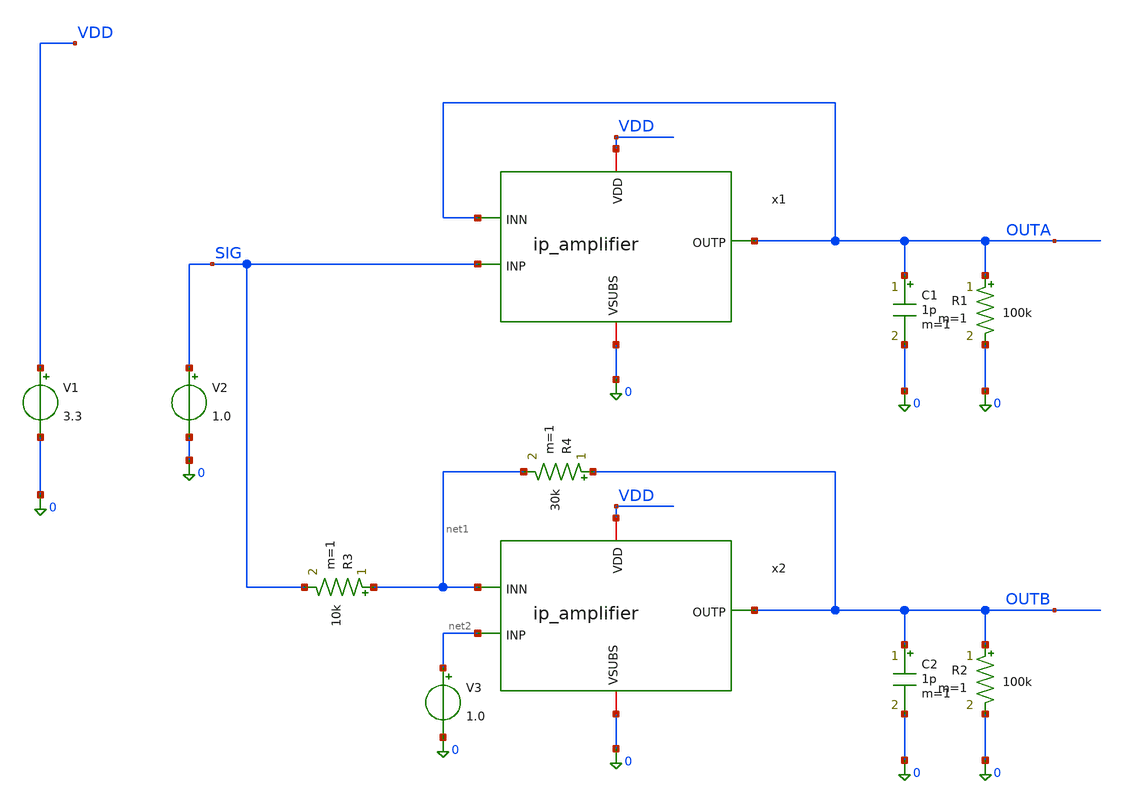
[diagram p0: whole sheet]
** sch_path: xschem/tb_amplifier_dc.sch
**.subckt tb_amplifier_dc
V1 VDD 0 3.3
x1 VDD OUTA SIG OUTA 0 ip_amplifier
V2 SIG 0 1.0
R1 OUTA 0 100k m=1
C1 OUTA 0 1p m=1
x2 VDD OUTB net2 net1 0 ip_amplifier
R2 OUTB 0 100k m=1
C2 OUTB 0 1p m=1
V3 net2 0 1.0
R3 net1 SIG 10k m=1
R4 OUTB net1 30k m=1
**** begin user architecture code

.lib $::180MCU_MODELS/sm141064.ngspice statistical
.lib $::180MCU_MODELS/sm141064.ngspice res_statistical
.lib $::180MCU_MODELS/sm141064.ngspice moscap_typical
.lib $::180MCU_MODELS/sm141064.ngspice diode_typical




.param sw_stat_global   = 1
.param sw_stat_mismatch = 1
.param mc_skew          = 1
.param res_mc_skew=3
.param cap_mc_skew=3
.param fnoicor=0

.control
	save all
	repeat 1
		mc_source
		dc V2 0 2 0.01
		write tb_amplifier_dc.raw
		set appendwrite
		reset
	end
	quit
.endc



**** end user architecture code
**.ends

* expanding   symbol:  ip_amplifier.sym # of pins=5
** sym_path: xschem/ip_amplifier.sym
** sch_path: xschem/ip_amplifier.sch
.subckt ip_amplifier VDD OUTP INP INN VSUBS
*.iopin VDD
*.iopin VSUBS
*.ipin INP
*.ipin INN
*.opin OUTP
XM1 net9 INP net7 VDD pfet_06v0 L=2u W=40u nf=1 ad='int((nf+1)/2) * W/nf * 0.18u' as='int((nf+2)/2) * W/nf * 0.18u'
+ pd='2*int((nf+1)/2) * (W/nf + 0.18u)' ps='2*int((nf+2)/2) * (W/nf + 0.18u)' nrd='0.18u / W' nrs='0.18u / W'
+ sa=0 sb=0 sd=0 m=1 par=1
XM2 net8 INN net7 VDD pfet_06v0 L=2u W=40u nf=1 ad='int((nf+1)/2) * W/nf * 0.18u' as='int((nf+2)/2) * W/nf * 0.18u'
+ pd='2*int((nf+1)/2) * (W/nf + 0.18u)' ps='2*int((nf+2)/2) * (W/nf + 0.18u)' nrd='0.18u / W' nrs='0.18u / W'
+ sa=0 sb=0 sd=0 m=1 par=1
XM5 net9 net1 VSUBS vsubs nfet_06v0 L=5u W=10u nf=1 ad='int((nf+1)/2) * W/nf * 0.18u' as='int((nf+2)/2) * W/nf * 0.18u'
+ pd='2*int((nf+1)/2) * (W/nf + 0.18u)' ps='2*int((nf+2)/2) * (W/nf + 0.18u)' nrd='0.18u / W' nrs='0.18u / W'
+ sa=0 sb=0 sd=0 m=1 par=1
XM6 net8 net1 VSUBS vsubs nfet_06v0 L=5u W=10u nf=1 ad='int((nf+1)/2) * W/nf * 0.18u' as='int((nf+2)/2) * W/nf * 0.18u'
+ pd='2*int((nf+1)/2) * (W/nf + 0.18u)' ps='2*int((nf+2)/2) * (W/nf + 0.18u)' nrd='0.18u / W' nrs='0.18u / W'
+ sa=0 sb=0 sd=0 m=1 par=1
XM3 net3 net1 VSUBS vsubs nfet_06v0 L=5u W=10u nf=1 ad='int((nf+1)/2) * W/nf * 0.18u' as='int((nf+2)/2) * W/nf * 0.18u'
+ pd='2*int((nf+1)/2) * (W/nf + 0.18u)' ps='2*int((nf+2)/2) * (W/nf + 0.18u)' nrd='0.18u / W' nrs='0.18u / W'
+ sa=0 sb=0 sd=0 m=1 par=1
XM4 net2 net1 VSUBS vsubs nfet_06v0 L=5u W=10u nf=1 ad='int((nf+1)/2) * W/nf * 0.18u' as='int((nf+2)/2) * W/nf * 0.18u'
+ pd='2*int((nf+1)/2) * (W/nf + 0.18u)' ps='2*int((nf+2)/2) * (W/nf + 0.18u)' nrd='0.18u / W' nrs='0.18u / W'
+ sa=0 sb=0 sd=0 m=1 par=1
XM7 net1 net1 net3 vsubs nfet_06v0 L=2u W=100u nf=1 ad='int((nf+1)/2) * W/nf * 0.18u' as='int((nf+2)/2) * W/nf * 0.18u'
+ pd='2*int((nf+1)/2) * (W/nf + 0.18u)' ps='2*int((nf+2)/2) * (W/nf + 0.18u)' nrd='0.18u / W' nrs='0.18u / W'
+ sa=0 sb=0 sd=0 m=1 par=1
XM8 net4 net1 net2 vsubs nfet_06v0 L=2u W=100u nf=1 ad='int((nf+1)/2) * W/nf * 0.18u' as='int((nf+2)/2) * W/nf * 0.18u'
+ pd='2*int((nf+1)/2) * (W/nf + 0.18u)' ps='2*int((nf+2)/2) * (W/nf + 0.18u)' nrd='0.18u / W' nrs='0.18u / W'
+ sa=0 sb=0 sd=0 m=1 par=1
I0 VDD net1 20u
XM9 net5 net4 VDD VDD pfet_06v0 L=5u W=30u nf=1 ad='int((nf+1)/2) * W/nf * 0.18u' as='int((nf+2)/2) * W/nf * 0.18u'
+ pd='2*int((nf+1)/2) * (W/nf + 0.18u)' ps='2*int((nf+2)/2) * (W/nf + 0.18u)' nrd='0.18u / W' nrs='0.18u / W'
+ sa=0 sb=0 sd=0 m=1 par=1
XM10 net6 net4 VDD VDD pfet_06v0 L=5u W=30u nf=1 ad='int((nf+1)/2) * W/nf * 0.18u' as='int((nf+2)/2) * W/nf * 0.18u'
+ pd='2*int((nf+1)/2) * (W/nf + 0.18u)' ps='2*int((nf+2)/2) * (W/nf + 0.18u)' nrd='0.18u / W' nrs='0.18u / W'
+ sa=0 sb=0 sd=0 m=1 par=1
XM11 net4 net4 net5 VDD pfet_06v0 L=2u W=100u nf=1 ad='int((nf+1)/2) * W/nf * 0.18u' as='int((nf+2)/2) * W/nf * 0.18u'
+ pd='2*int((nf+1)/2) * (W/nf + 0.18u)' ps='2*int((nf+2)/2) * (W/nf + 0.18u)' nrd='0.18u / W' nrs='0.18u / W'
+ sa=0 sb=0 sd=0 m=1 par=1
XM12 net7 net4 net6 VDD pfet_06v0 L=2u W=100u nf=1 ad='int((nf+1)/2) * W/nf * 0.18u' as='int((nf+2)/2) * W/nf * 0.18u'
+ pd='2*int((nf+1)/2) * (W/nf + 0.18u)' ps='2*int((nf+2)/2) * (W/nf + 0.18u)' nrd='0.18u / W' nrs='0.18u / W'
+ sa=0 sb=0 sd=0 m=1 par=1
XM13 net10 net1 net8 vsubs nfet_06v0 L=2u W=100u nf=1 ad='int((nf+1)/2) * W/nf * 0.18u' as='int((nf+2)/2) * W/nf * 0.18u'
+ pd='2*int((nf+1)/2) * (W/nf + 0.18u)' ps='2*int((nf+2)/2) * (W/nf + 0.18u)' nrd='0.18u / W' nrs='0.18u / W'
+ sa=0 sb=0 sd=0 m=1 par=1
XM14 net11 net1 net9 vsubs nfet_06v0 L=2u W=100u nf=1 ad='int((nf+1)/2) * W/nf * 0.18u' as='int((nf+2)/2) * W/nf * 0.18u'
+ pd='2*int((nf+1)/2) * (W/nf + 0.18u)' ps='2*int((nf+2)/2) * (W/nf + 0.18u)' nrd='0.18u / W' nrs='0.18u / W'
+ sa=0 sb=0 sd=0 m=1 par=1
XM15 net10 net10 VDD VDD pfet_06v0 L=3u W=60u nf=1 ad='int((nf+1)/2) * W/nf * 0.18u' as='int((nf+2)/2) * W/nf * 0.18u'
+ pd='2*int((nf+1)/2) * (W/nf + 0.18u)' ps='2*int((nf+2)/2) * (W/nf + 0.18u)' nrd='0.18u / W' nrs='0.18u / W'
+ sa=0 sb=0 sd=0 m=1 par=1
XM16 net11 net10 VDD VDD pfet_06v0 L=3u W=60u nf=1 ad='int((nf+1)/2) * W/nf * 0.18u' as='int((nf+2)/2) * W/nf * 0.18u'
+ pd='2*int((nf+1)/2) * (W/nf + 0.18u)' ps='2*int((nf+2)/2) * (W/nf + 0.18u)' nrd='0.18u / W' nrs='0.18u / W'
+ sa=0 sb=0 sd=0 m=1 par=1
XM17 OUTP net11 VDD VDD pfet_06v0 L=0.5u W=90u nf=1 ad='int((nf+1)/2) * W/nf * 0.18u' as='int((nf+2)/2) * W/nf * 0.18u'
+ pd='2*int((nf+1)/2) * (W/nf + 0.18u)' ps='2*int((nf+2)/2) * (W/nf + 0.18u)' nrd='0.18u / W' nrs='0.18u / W'
+ sa=0 sb=0 sd=0 m=1 par=1
XM18 OUTP net9 VSUBS vsubs nfet_06v0 L=5u W=30u nf=1 ad='int((nf+1)/2) * W/nf * 0.18u' as='int((nf+2)/2) * W/nf * 0.18u'
+ pd='2*int((nf+1)/2) * (W/nf + 0.18u)' ps='2*int((nf+2)/2) * (W/nf + 0.18u)' nrd='0.18u / W' nrs='0.18u / W'
+ sa=0 sb=0 sd=0 m=1 par=1
C1 OUTP net11 1p m=1
.ends

.end
